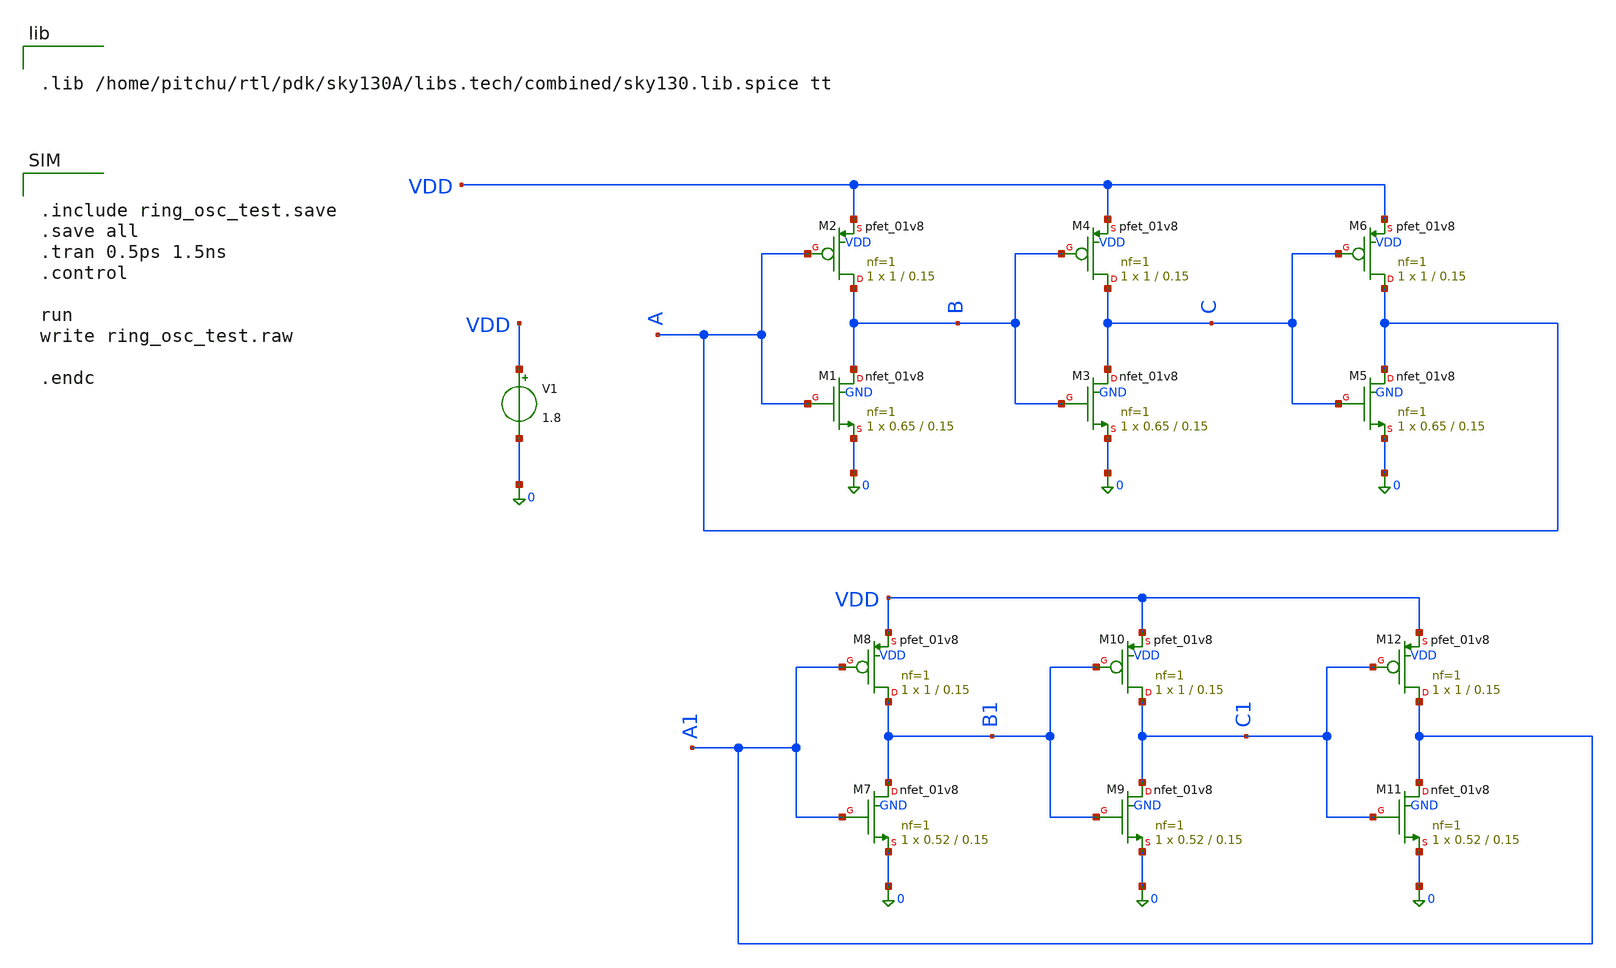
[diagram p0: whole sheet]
** sch_path: schem/ring_osc_test.sch
**.subckt ring_osc_test
XM1 B A 0 GND sky130_fd_pr__nfet_01v8 L=0.15 W=0.65 nf=1 ad='int((1 + 1)/2) * 0.65 / 1 * 0.29' as='int((1 + 2)/2) * 0.65 / 1 * 0.29'
+ pd='2*int((1 + 1)/2) * (0.65 / 1 + 0.29)' ps='2*int((1 + 2)/2) * (0.65 / 1 + 0.29)' nrd='0.29 / 0.65 '
+ nrs='0.29 / 0.65 ' sa=0 sb=0 sd=0 mult=1 m=1
XM2 B A VDD VDD sky130_fd_pr__pfet_01v8 L=0.15 W=1 nf=1 ad='int((1 + 1)/2) * 1 / 1 * 0.29' as='int((1 + 2)/2) * 1 / 1 * 0.29'
+ pd='2*int((1 + 1)/2) * (1 / 1 + 0.29)' ps='2*int((1 + 2)/2) * (1 / 1 + 0.29)' nrd='0.29 / 1 ' nrs='0.29 / 1 '
+ sa=0 sb=0 sd=0 mult=1 m=1
V1 VDD 0 1.8
XM3 C B 0 GND sky130_fd_pr__nfet_01v8 L=0.15 W=0.65 nf=1 ad='int((1 + 1)/2) * 0.65 / 1 * 0.29' as='int((1 + 2)/2) * 0.65 / 1 * 0.29'
+ pd='2*int((1 + 1)/2) * (0.65 / 1 + 0.29)' ps='2*int((1 + 2)/2) * (0.65 / 1 + 0.29)' nrd='0.29 / 0.65 '
+ nrs='0.29 / 0.65 ' sa=0 sb=0 sd=0 mult=1 m=1
XM4 C B VDD VDD sky130_fd_pr__pfet_01v8 L=0.15 W=1 nf=1 ad='int((1 + 1)/2) * 1 / 1 * 0.29' as='int((1 + 2)/2) * 1 / 1 * 0.29'
+ pd='2*int((1 + 1)/2) * (1 / 1 + 0.29)' ps='2*int((1 + 2)/2) * (1 / 1 + 0.29)' nrd='0.29 / 1 ' nrs='0.29 / 1 '
+ sa=0 sb=0 sd=0 mult=1 m=1
XM5 A C 0 GND sky130_fd_pr__nfet_01v8 L=0.15 W=0.65 nf=1 ad='int((1 + 1)/2) * 0.65 / 1 * 0.29' as='int((1 + 2)/2) * 0.65 / 1 * 0.29'
+ pd='2*int((1 + 1)/2) * (0.65 / 1 + 0.29)' ps='2*int((1 + 2)/2) * (0.65 / 1 + 0.29)' nrd='0.29 / 0.65 '
+ nrs='0.29 / 0.65 ' sa=0 sb=0 sd=0 mult=1 m=1
XM6 A C VDD VDD sky130_fd_pr__pfet_01v8 L=0.15 W=1 nf=1 ad='int((1 + 1)/2) * 1 / 1 * 0.29' as='int((1 + 2)/2) * 1 / 1 * 0.29'
+ pd='2*int((1 + 1)/2) * (1 / 1 + 0.29)' ps='2*int((1 + 2)/2) * (1 / 1 + 0.29)' nrd='0.29 / 1 ' nrs='0.29 / 1 '
+ sa=0 sb=0 sd=0 mult=1 m=1
XM7 B1 A1 0 GND sky130_fd_pr__nfet_01v8 L=0.15 W=0.52 nf=1 ad='int((1 + 1)/2) * 0.52 / 1 * 0.29' as='int((1 + 2)/2) * 0.52 / 1 * 0.29'
+ pd='2*int((1 + 1)/2) * (0.52 / 1 + 0.29)' ps='2*int((1 + 2)/2) * (0.52 / 1 + 0.29)' nrd='0.29 / 0.52 '
+ nrs='0.29 / 0.52 ' sa=0 sb=0 sd=0 mult=1 m=1
XM8 B1 A1 VDD VDD sky130_fd_pr__pfet_01v8 L=0.15 W=1 nf=1 ad='int((1 + 1)/2) * 1 / 1 * 0.29' as='int((1 + 2)/2) * 1 / 1 * 0.29'
+ pd='2*int((1 + 1)/2) * (1 / 1 + 0.29)' ps='2*int((1 + 2)/2) * (1 / 1 + 0.29)' nrd='0.29 / 1 ' nrs='0.29 / 1 '
+ sa=0 sb=0 sd=0 mult=1 m=1
XM9 C1 B1 0 GND sky130_fd_pr__nfet_01v8 L=0.15 W=0.52 nf=1 ad='int((1 + 1)/2) * 0.52 / 1 * 0.29' as='int((1 + 2)/2) * 0.52 / 1 * 0.29'
+ pd='2*int((1 + 1)/2) * (0.52 / 1 + 0.29)' ps='2*int((1 + 2)/2) * (0.52 / 1 + 0.29)' nrd='0.29 / 0.52 '
+ nrs='0.29 / 0.52 ' sa=0 sb=0 sd=0 mult=1 m=1
XM10 C1 B1 VDD VDD sky130_fd_pr__pfet_01v8 L=0.15 W=1 nf=1 ad='int((1 + 1)/2) * 1 / 1 * 0.29' as='int((1 + 2)/2) * 1 / 1 * 0.29'
+ pd='2*int((1 + 1)/2) * (1 / 1 + 0.29)' ps='2*int((1 + 2)/2) * (1 / 1 + 0.29)' nrd='0.29 / 1 ' nrs='0.29 / 1 '
+ sa=0 sb=0 sd=0 mult=1 m=1
XM11 A1 C1 0 GND sky130_fd_pr__nfet_01v8 L=0.15 W=0.52 nf=1 ad='int((1 + 1)/2) * 0.52 / 1 * 0.29' as='int((1 + 2)/2) * 0.52 / 1 * 0.29'
+ pd='2*int((1 + 1)/2) * (0.52 / 1 + 0.29)' ps='2*int((1 + 2)/2) * (0.52 / 1 + 0.29)' nrd='0.29 / 0.52 '
+ nrs='0.29 / 0.52 ' sa=0 sb=0 sd=0 mult=1 m=1
XM12 A1 C1 VDD VDD sky130_fd_pr__pfet_01v8 L=0.15 W=1 nf=1 ad='int((1 + 1)/2) * 1 / 1 * 0.29' as='int((1 + 2)/2) * 1 / 1 * 0.29'
+ pd='2*int((1 + 1)/2) * (1 / 1 + 0.29)' ps='2*int((1 + 2)/2) * (1 / 1 + 0.29)' nrd='0.29 / 1 ' nrs='0.29 / 1 '
+ sa=0 sb=0 sd=0 mult=1 m=1
**** begin user architecture code


.include ring_osc_test.save
.save all
.tran 0.5ps 1.5ns
.control

run
write ring_osc_test.raw

.endc




.lib /home/pitchu/rtl/pdk/sky130A/libs.tech/combined/sky130.lib.spice tt


**** end user architecture code
**.ends
.end
